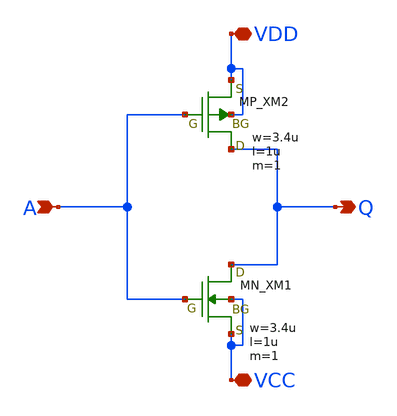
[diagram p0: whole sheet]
** sch_path: member_project/inverter/rikulh/inverter.sch
**.subckt inverter VCC A Q VDD
*.iopin VCC
*.ipin A
*.opin Q
*.iopin VDD
XM1 Q A VCC VCC NMOS w=3.4u l=1u as=0 ad=0 ps=0 pd=0 nrd=0 nrs=0 m=1
XM2 Q A VDD VDD PMOS w=3.4u l=1u as=0 ad=0 ps=0 pd=0 nrd=0 nrs=0 m=1
**.ends
.end
